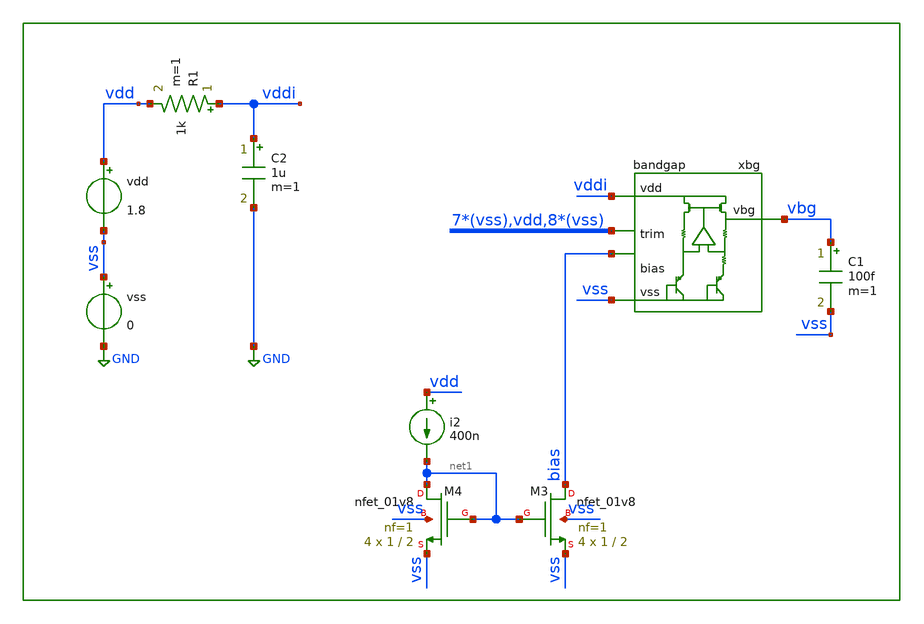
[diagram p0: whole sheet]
** sch_path: xschem/tb/bandgap/tr_bandgap_startup.sch
**.subckt tr_bandgap_startup
xbg vddi vbg vss bias vss vss vss vss vss vss vss vdd vss vss vss vss vss vss vss vss bandgap
vdd vdd vss 1.8
vss vss GND 0
C1 vbg vss 100f m=1
i2 vdd net1 400n
XM3 bias net1 vss vss sky130_fd_pr__nfet_01v8 L=2 W=1 nf=1 ad='int((nf+1)/2) * W/nf * 0.29' as='int((nf+2)/2) * W/nf * 0.29'
+ pd='2*int((nf+1)/2) * (W/nf + 0.29)' ps='2*int((nf+2)/2) * (W/nf + 0.29)' nrd='0.29 / W' nrs='0.29 / W'
+ sa=0 sb=0 sd=0 mult=4 m=4
XM4 net1 net1 vss vss sky130_fd_pr__nfet_01v8 L=2 W=1 nf=1 ad='int((nf+1)/2) * W/nf * 0.29' as='int((nf+2)/2) * W/nf * 0.29'
+ pd='2*int((nf+1)/2) * (W/nf + 0.29)' ps='2*int((nf+2)/2) * (W/nf + 0.29)' nrd='0.29 / W' nrs='0.29 / W'
+ sa=0 sb=0 sd=0 mult=4 m=4
R1 vddi vdd 1k m=1
C2 vddi GND 1u m=1
**** begin user architecture code

* tr bandgap startup

.param MC_SWITCH=0

.control
save all
tran 1u 10m uic
.endc
.end



* FET CORNERS
.include $::SKYWATER_MODELS/corners/tt.spice
*.include $::SKYWATER_MODELS/corners/ff.spice
*.include $::SKYWATER_MODELS/corners/ss.spice
*.include $::SKYWATER_MODELS/corners/sf.spice
*.include $::SKYWATER_MODELS/corners/fs.spice

* TT + R + C
*.include $::SKYWATER_MODELS/corners/tt_rmax_cmax.spice
*.include $::SKYWATER_MODELS/corners/tt_rmin_cmin.spice
*.include $::SKYWATER_MODELS/corners/tt_rmax_cmin.spice
*.include $::SKYWATER_MODELS/corners/tt_rmin_cmax.spice

* FF + R + C
*.include $::SKYWATER_MODELS/corners/ff_rmax_cmax.spice
*.include $::SKYWATER_MODELS/corners/ff_rmin_cmin.spice
*.include $::SKYWATER_MODELS/corners/ff_rmax_cmin.spice
*.include $::SKYWATER_MODELS/corners/ff_rmin_cmax.spice


* SS + R + C
*.include $::SKYWATER_MODELS/corners/ss_rmax_cmax.spice
*.include $::SKYWATER_MODELS/corners/ss_rmin_cmin.spice
*.include $::SKYWATER_MODELS/corners/ss_rmax_cmin.spice
*.include $::SKYWATER_MODELS/corners/ss_rmin_cmax.spice

* SF + R + C
*.include $::SKYWATER_MODELS/corners/sf_rmax_cmax.spice
*.include $::SKYWATER_MODELS/corners/sf_rmin_cmin.spice
*.include $::SKYWATER_MODELS/corners/sf_rmax_cmin.spice
*.include $::SKYWATER_MODELS/corners/sf_rmin_cmax.spice

* FS + R + C
*.include $::SKYWATER_MODELS/corners/fs_rmax_cmax.spice
*.include $::SKYWATER_MODELS/corners/fs_rmin_cmin.spice
*.include $::SKYWATER_MODELS/corners/fs_rmax_cmin.spice
*.include $::SKYWATER_MODELS/corners/fs_rmin_cmax.spice

**** end user architecture code
**.ends
.GLOBAL GND
.end
